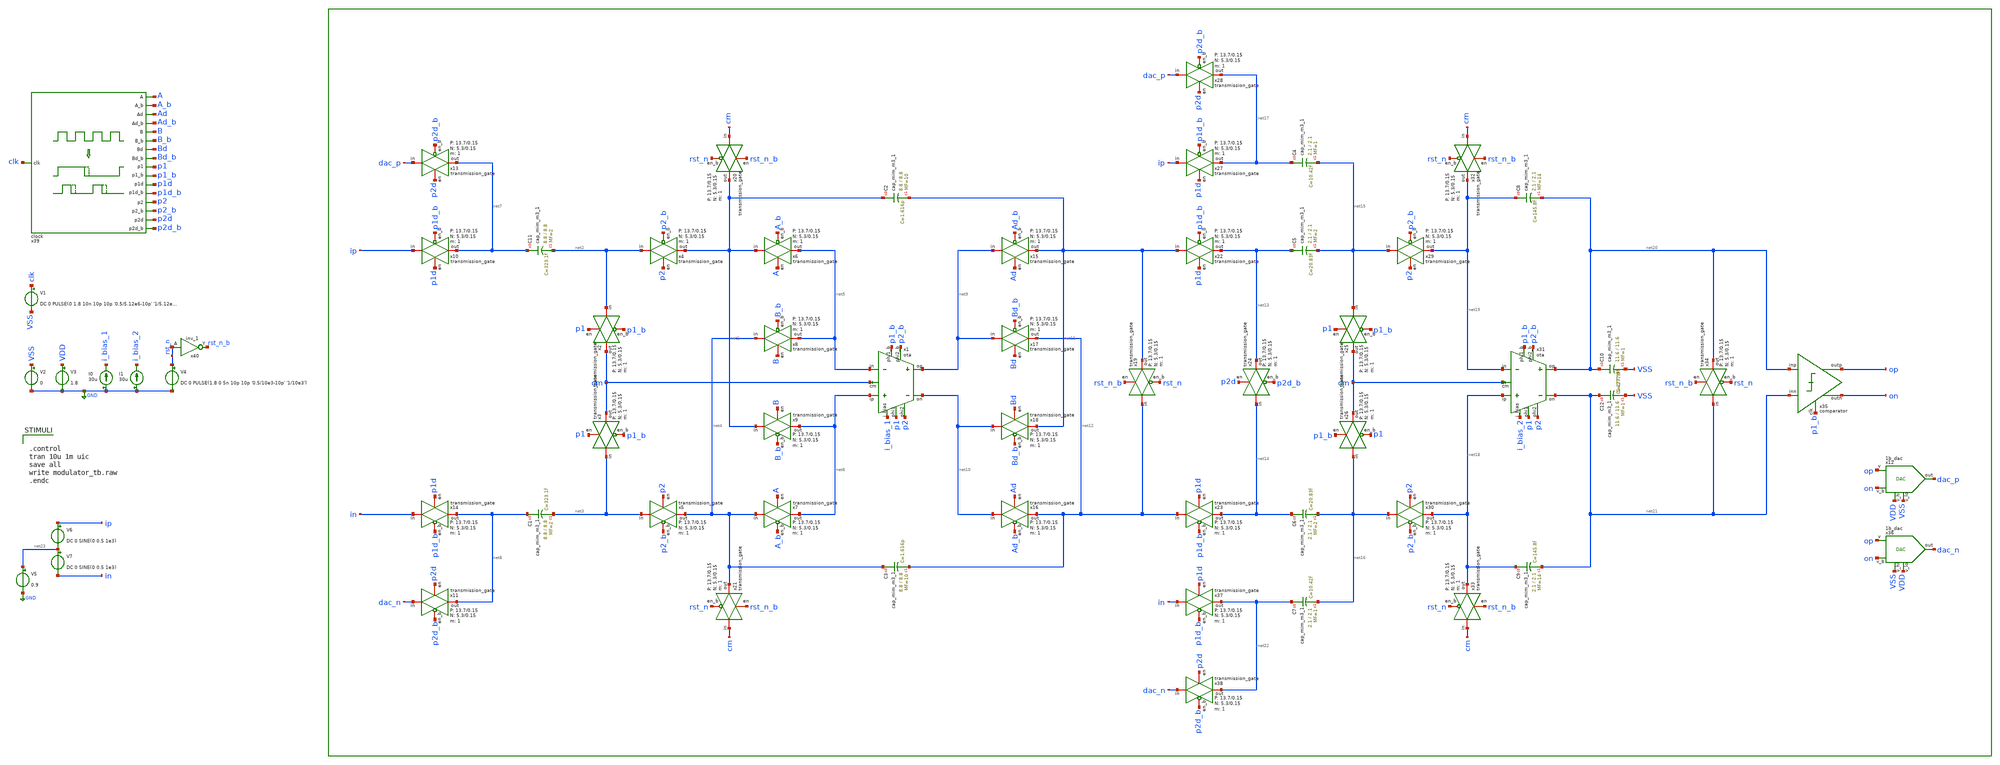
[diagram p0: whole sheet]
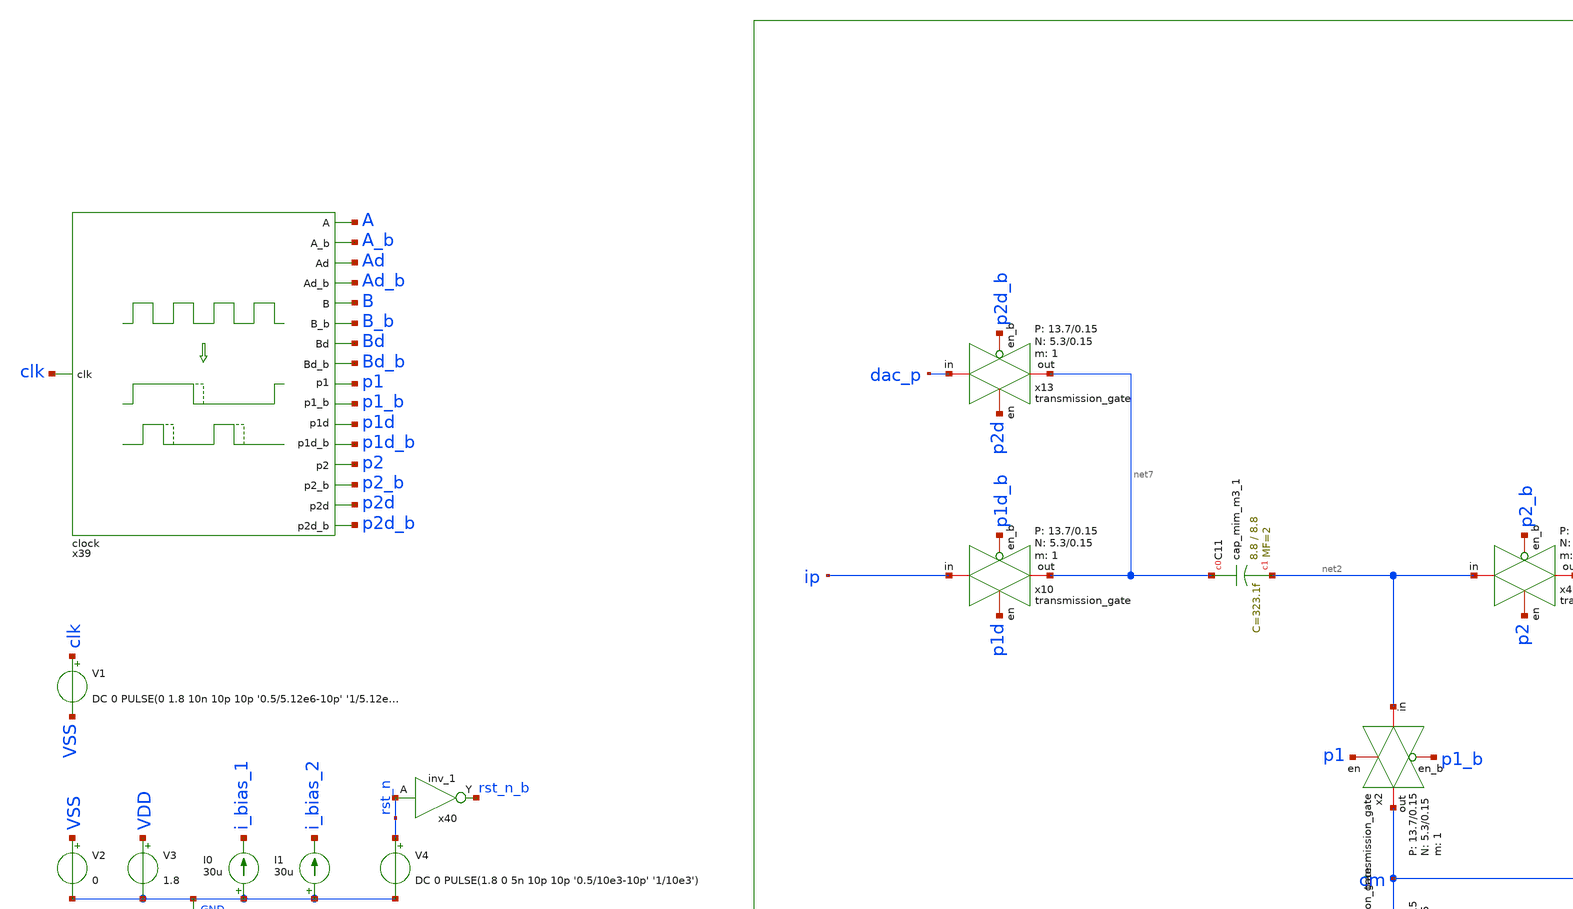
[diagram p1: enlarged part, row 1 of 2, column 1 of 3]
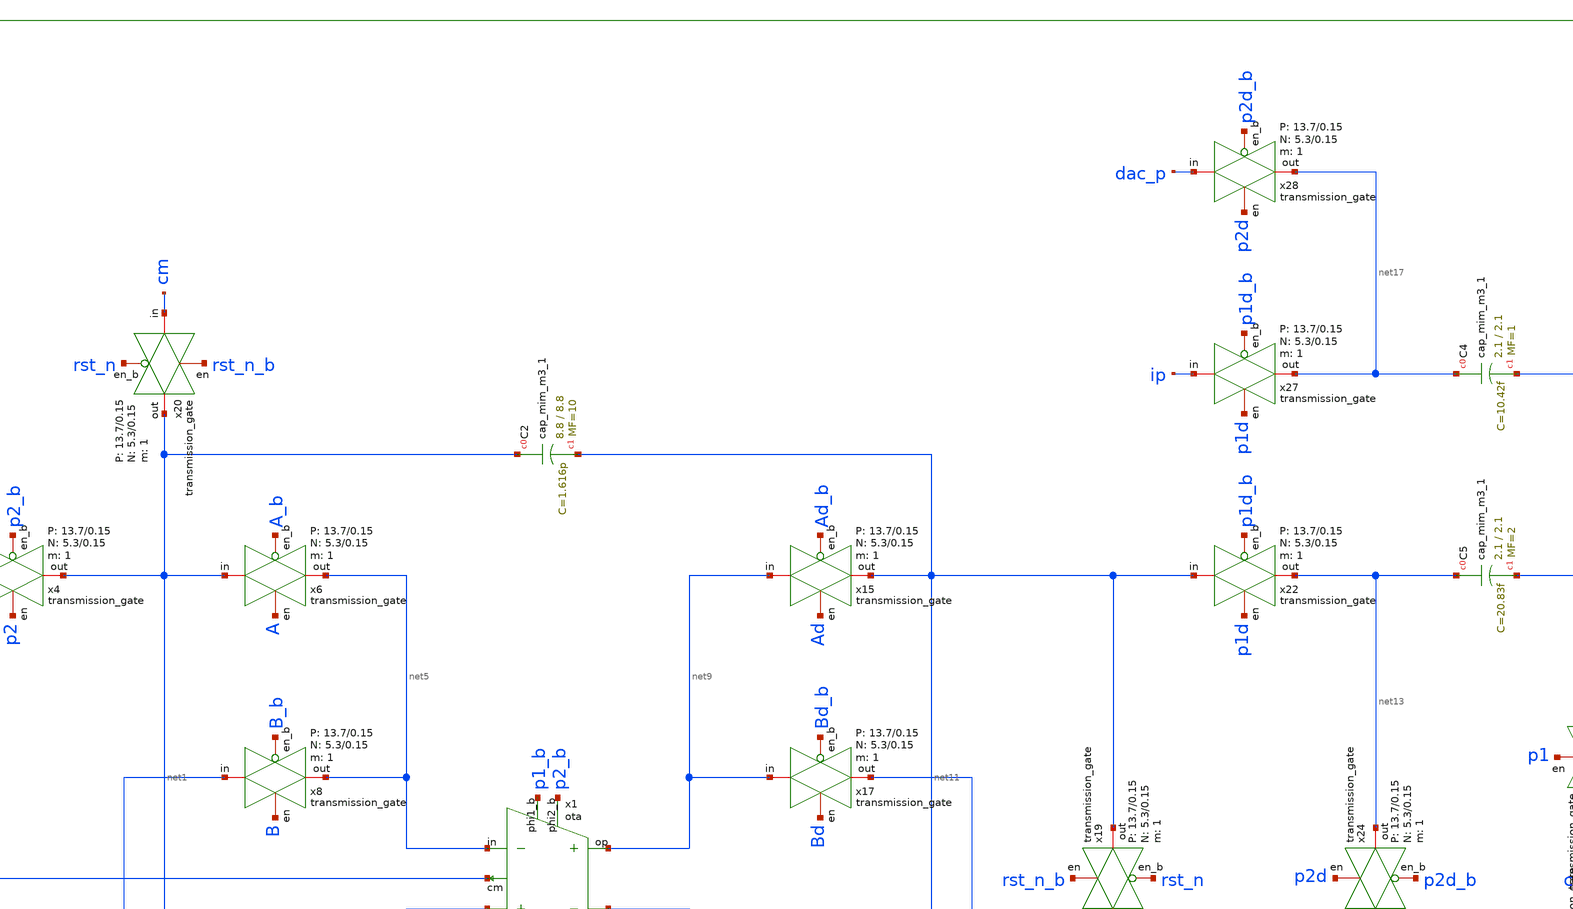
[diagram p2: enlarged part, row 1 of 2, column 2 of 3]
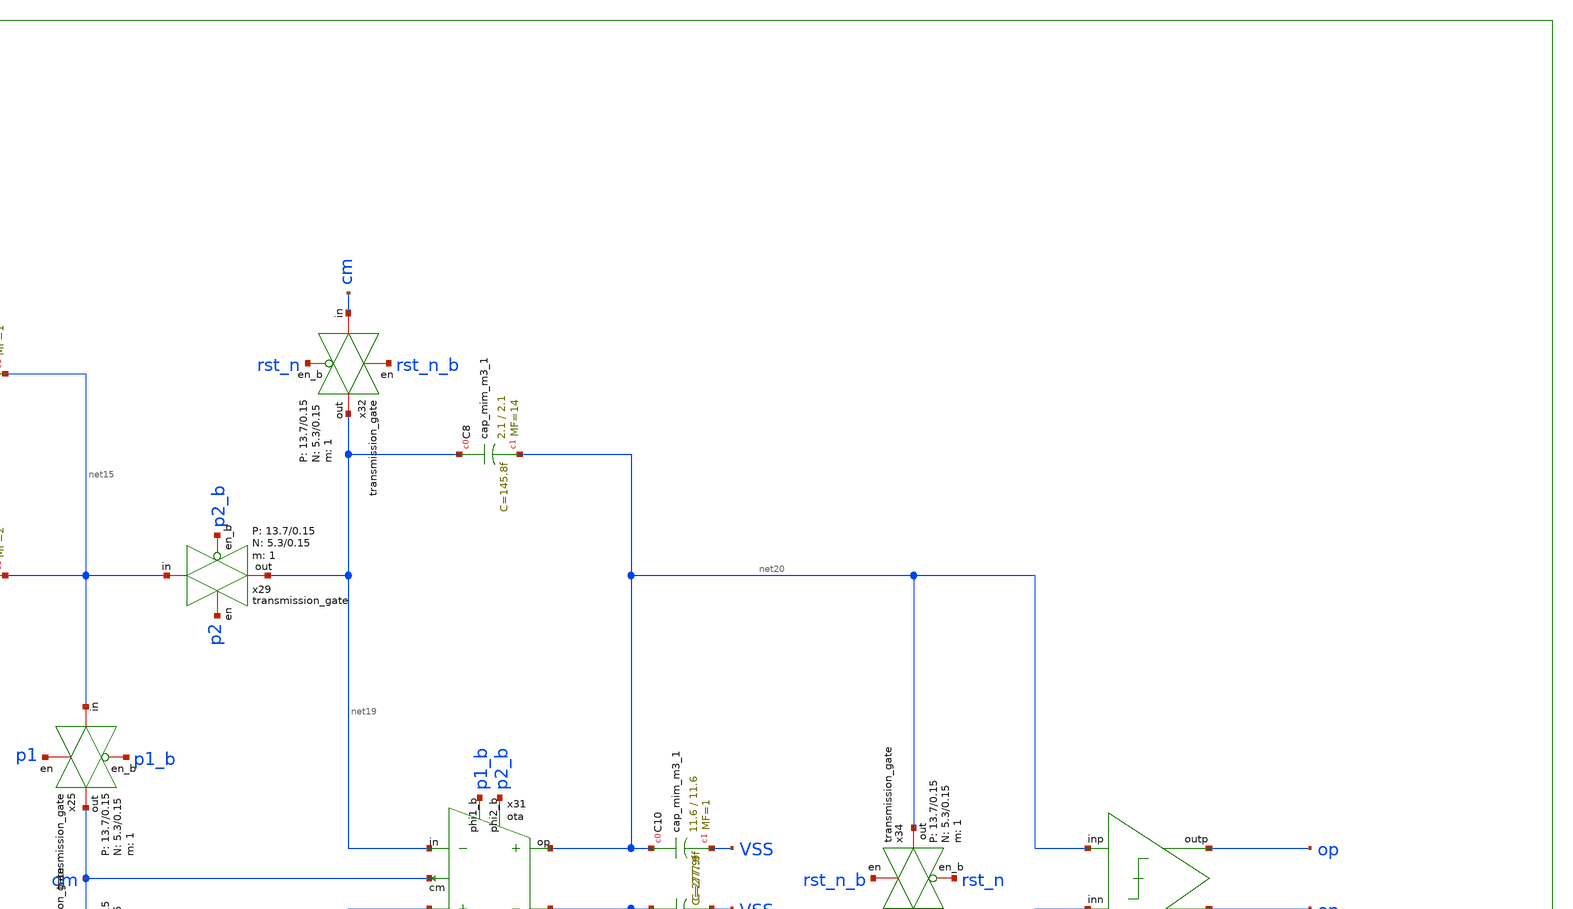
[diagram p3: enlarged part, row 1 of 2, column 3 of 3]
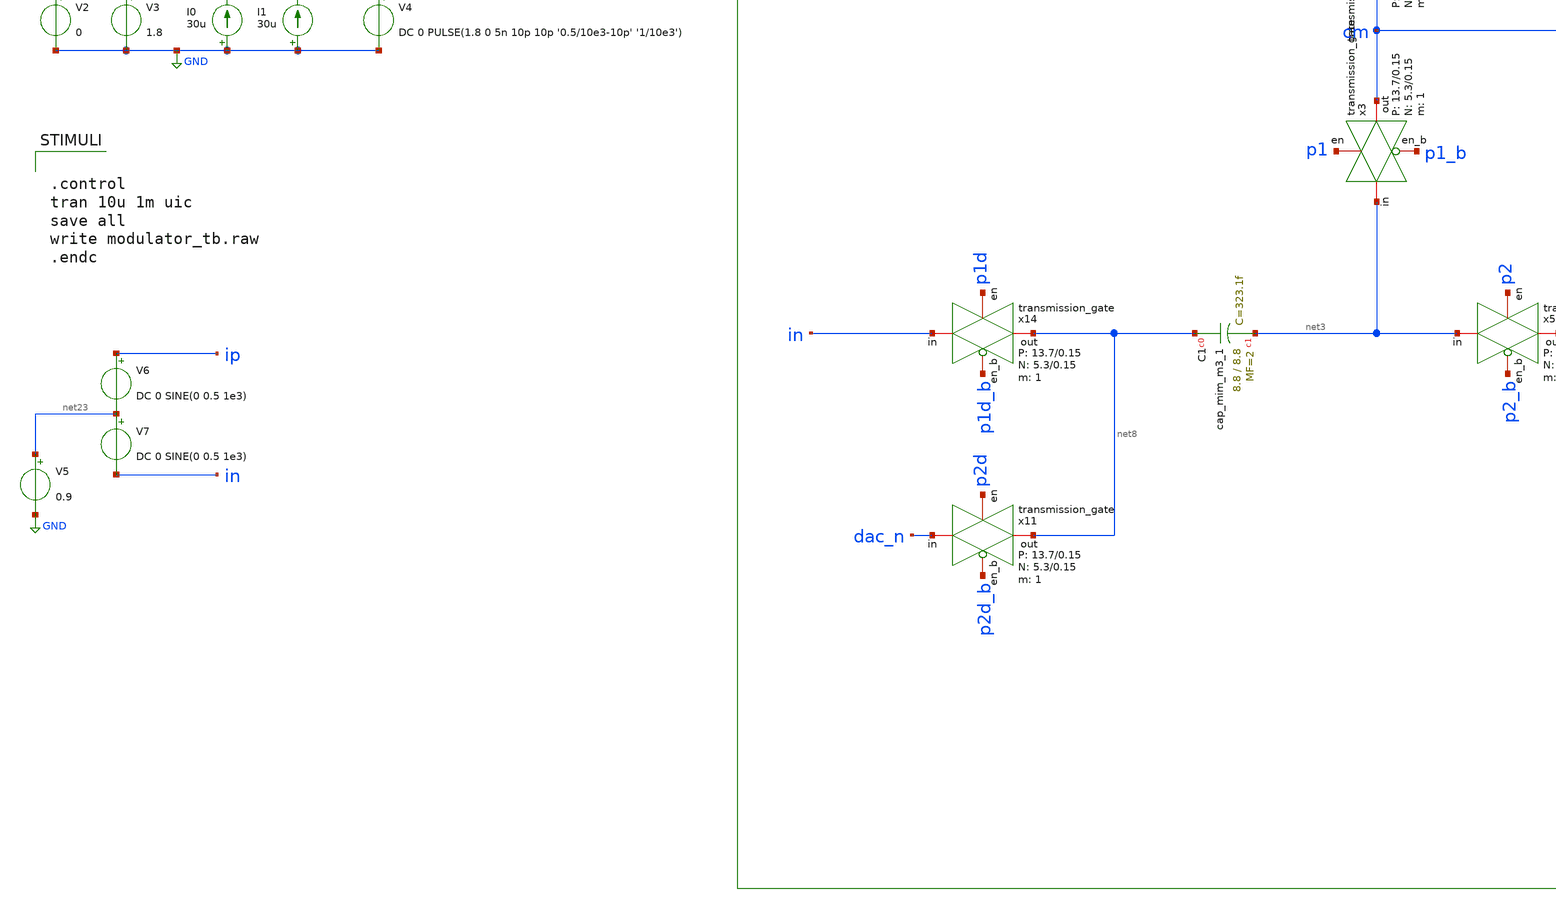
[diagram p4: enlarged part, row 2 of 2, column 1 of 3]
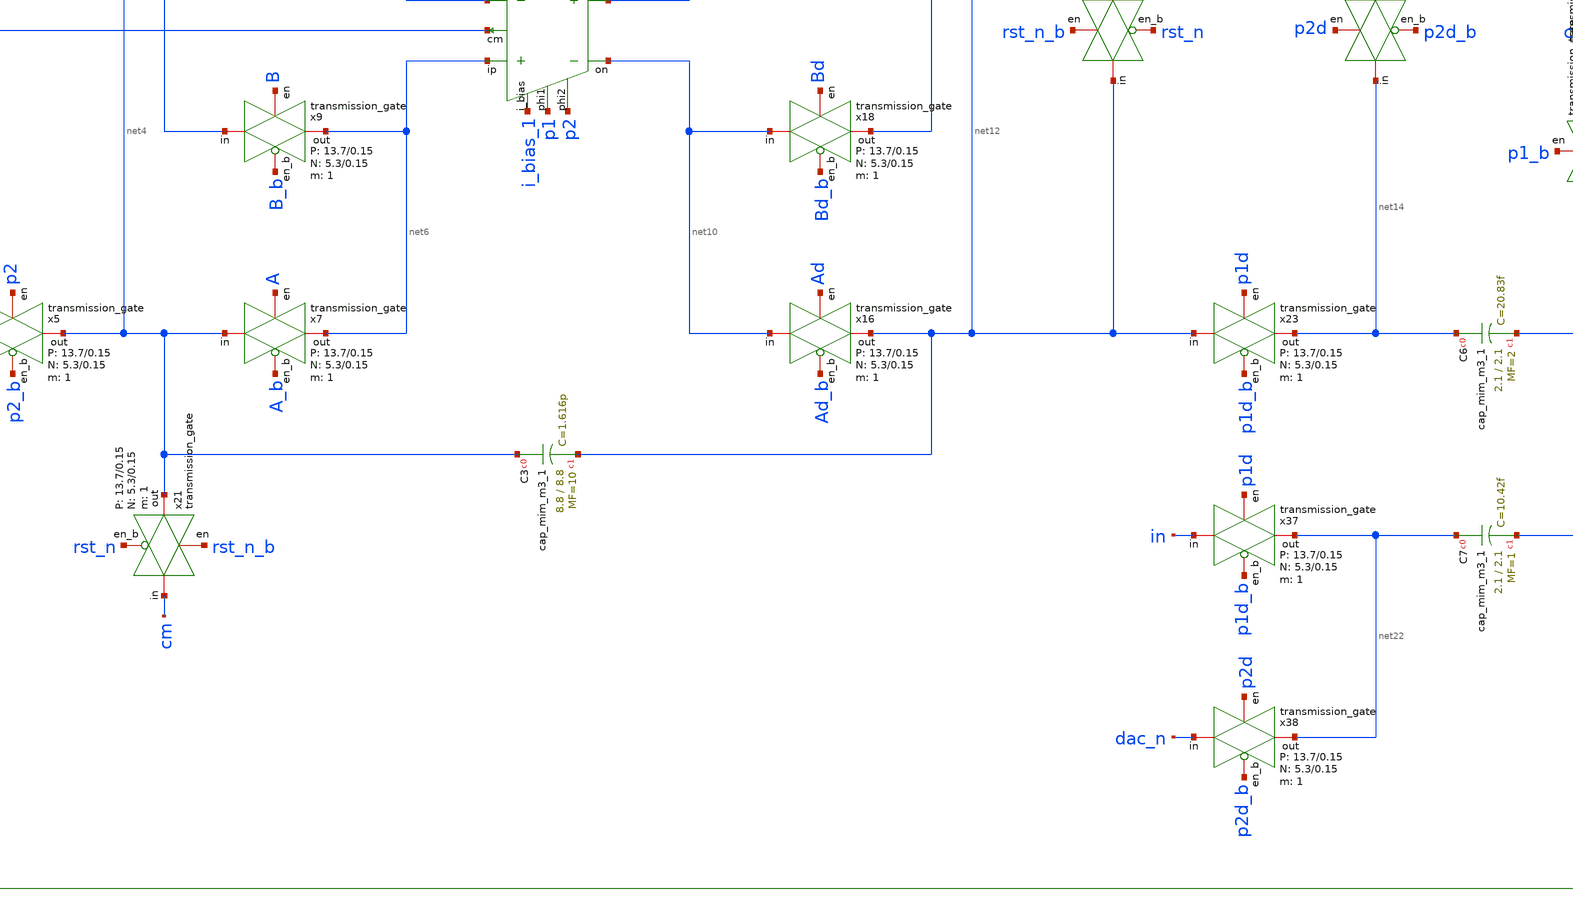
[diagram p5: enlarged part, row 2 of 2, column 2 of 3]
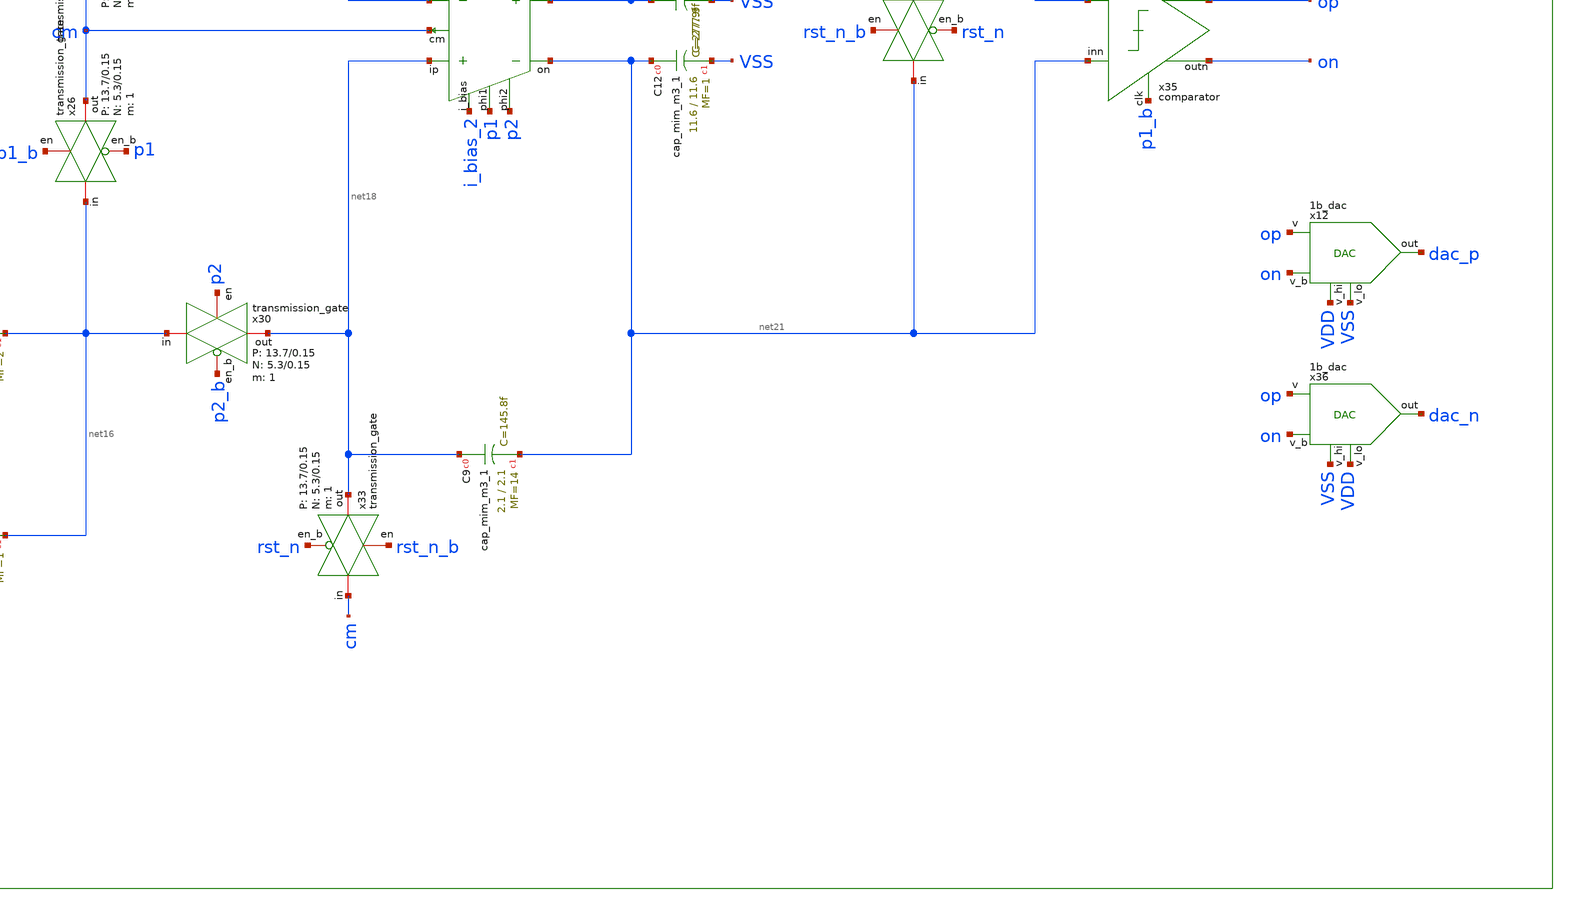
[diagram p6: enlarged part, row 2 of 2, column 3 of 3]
** sch_path: verification/schematic/modulator_ideal_clock.sch
**.subckt modulator_ideal_clock
x1 i_bias_1 net6 net5 p1 p1_b p2 p2_b net9 net10 cm 50 350 VDD VSS ota
x4 net2 net1 p2 p2_b VDD VSS 1 5.3 0.15 13.7 0.15 transmission_gate
x5 net3 net4 p2 p2_b VDD VSS 1 5.3 0.15 13.7 0.15 transmission_gate
x6 net1 net5 A A_b VDD VSS 1 5.3 0.15 13.7 0.15 transmission_gate
x7 net4 net6 A A_b VDD VSS 1 5.3 0.15 13.7 0.15 transmission_gate
x8 net4 net5 B B_b VDD VSS 1 5.3 0.15 13.7 0.15 transmission_gate
x9 net1 net6 B B_b VDD VSS 1 5.3 0.15 13.7 0.15 transmission_gate
x2 net2 cm p1 p1_b VDD VSS 1 5.3 0.15 13.7 0.15 transmission_gate
x3 net3 cm p1 p1_b VDD VSS 1 5.3 0.15 13.7 0.15 transmission_gate
x10 ip net7 p1d p1d_b VDD VSS 1 5.3 0.15 13.7 0.15 transmission_gate
x11 dac_n net8 p2d p2d_b VDD VSS 1 5.3 0.15 13.7 0.15 transmission_gate
x12 VDD VSS op dac_p on VDD VSS 1b_dac
x13 dac_p net7 p2d p2d_b VDD VSS 1 5.3 0.15 13.7 0.15 transmission_gate
x14 in net8 p1d p1d_b VDD VSS 1 5.3 0.15 13.7 0.15 transmission_gate
x15 net9 net11 Ad Ad_b VDD VSS 1 5.3 0.15 13.7 0.15 transmission_gate
x16 net10 net12 Ad Ad_b VDD VSS 1 5.3 0.15 13.7 0.15 transmission_gate
x17 net9 net12 Bd Bd_b VDD VSS 1 5.3 0.15 13.7 0.15 transmission_gate
x18 net10 net11 Bd Bd_b VDD VSS 1 5.3 0.15 13.7 0.15 transmission_gate
x19 net12 net11 rst_n_b rst_n VDD VSS 1 5.3 0.15 13.7 0.15 transmission_gate
x20 cm net1 rst_n_b rst_n VDD VSS 1 5.3 0.15 13.7 0.15 transmission_gate
x21 cm net4 rst_n_b rst_n VDD VSS 1 5.3 0.15 13.7 0.15 transmission_gate
x22 net11 net13 p1d p1d_b VDD VSS 1 5.3 0.15 13.7 0.15 transmission_gate
x23 net12 net14 p1d p1d_b VDD VSS 1 5.3 0.15 13.7 0.15 transmission_gate
x24 net14 net13 p2d p2d_b VDD VSS 1 5.3 0.15 13.7 0.15 transmission_gate
x25 net15 cm p1 p1_b VDD VSS 1 5.3 0.15 13.7 0.15 transmission_gate
x26 net16 cm p1_b p1 VDD VSS 1 5.3 0.15 13.7 0.15 transmission_gate
x27 ip net17 p1d p1d_b VDD VSS 1 5.3 0.15 13.7 0.15 transmission_gate
x28 dac_p net17 p2d p2d_b VDD VSS 1 5.3 0.15 13.7 0.15 transmission_gate
x29 net15 net19 p2 p2_b VDD VSS 1 5.3 0.15 13.7 0.15 transmission_gate
x30 net16 net18 p2 p2_b VDD VSS 1 5.3 0.15 13.7 0.15 transmission_gate
x31 i_bias_2 net18 net19 p1 p1_b p2 p2_b net20 net21 cm 50 350 VDD VSS ota
x32 cm net19 rst_n_b rst_n VDD VSS 1 5.3 0.15 13.7 0.15 transmission_gate
x33 cm net18 rst_n_b rst_n VDD VSS 1 5.3 0.15 13.7 0.15 transmission_gate
x34 net21 net20 rst_n_b rst_n VDD VSS 1 5.3 0.15 13.7 0.15 transmission_gate
x35 net20 net21 op p1_b on VDD VSS comparator
x36 VSS VDD op dac_n on VDD VSS 1b_dac
x37 in net22 p1d p1d_b VDD VSS 1 5.3 0.15 13.7 0.15 transmission_gate
x38 dac_n net22 p2d p2d_b VDD VSS 1 5.3 0.15 13.7 0.15 transmission_gate
x39 A A_b Ad Ad_b Bd_b Bd B_b B p2 p2_b p2d clk p2d_b p1d_b p1d p1_b p1 VDD VSS clock
V1 clk VSS DC 0 PULSE(0 1.8 10n 10p 10p '0.5/5.12e6-10p' '1/5.12e6')
V2 VSS GND 0
V3 VDD GND 1.8
I0 GND i_bias_1 30u
I1 GND i_bias_2 30u
V4 rst_n GND DC 0 PULSE(1.8 0 5n 10p 10p '0.5/10e3-10p' '1/10e3')
x40 rst_n GND GND VDD VDD rst_n_b sky130_fd_sc_hd__inv_1
V5 net23 GND 0.9
V6 ip net23 DC 0 SINE(0 0.5 1e3)
V7 net23 in DC 0 SINE(0 0.5 1e3)
XC11 net7 net2 sky130_fd_pr__cap_mim_m3_1 W=8.8 L=8.8 MF=2 m=2
XC1 net8 net3 sky130_fd_pr__cap_mim_m3_1 W=8.8 L=8.8 MF=2 m=2
XC2 net1 net11 sky130_fd_pr__cap_mim_m3_1 W=8.8 L=8.8 MF=10 m=10
XC3 net4 net12 sky130_fd_pr__cap_mim_m3_1 W=8.8 L=8.8 MF=10 m=10
XC4 net17 net15 sky130_fd_pr__cap_mim_m3_1 W=2.1 L=2.1 MF=1 m=1
XC5 net13 net15 sky130_fd_pr__cap_mim_m3_1 W=2.1 L=2.1 MF=2 m=2
XC6 net14 net16 sky130_fd_pr__cap_mim_m3_1 W=2.1 L=2.1 MF=2 m=2
XC7 net22 net16 sky130_fd_pr__cap_mim_m3_1 W=2.1 L=2.1 MF=1 m=1
XC8 net19 net20 sky130_fd_pr__cap_mim_m3_1 W=2.1 L=2.1 MF=14 m=14
XC9 net18 net21 sky130_fd_pr__cap_mim_m3_1 W=2.1 L=2.1 MF=14 m=14
XC10 net20 VSS sky130_fd_pr__cap_mim_m3_1 W=11.6 L=11.6 MF=1 m=1
XC12 net21 VSS sky130_fd_pr__cap_mim_m3_1 W=11.6 L=11.6 MF=1 m=1
**** begin user architecture code

** opencircuitdesign pdks install
.lib /farmshare/home/classes/ee/372/PDKs/open_pdks_1.0.310/sky130/sky130A/libs.tech/ngspice/sky130.lib.spice tt
.inc /farmshare/home/classes/ee/372/PDKs/open_pdks_1.0.310/sky130/sky130A/libs.ref/sky130_fd_sc_hd/spice/sky130_fd_sc_hd.spice



.control
tran 10u 1m uic
save all
write modulator_tb.raw
.endc


**** end user architecture code
**.ends
.GLOBAL GND
.end
